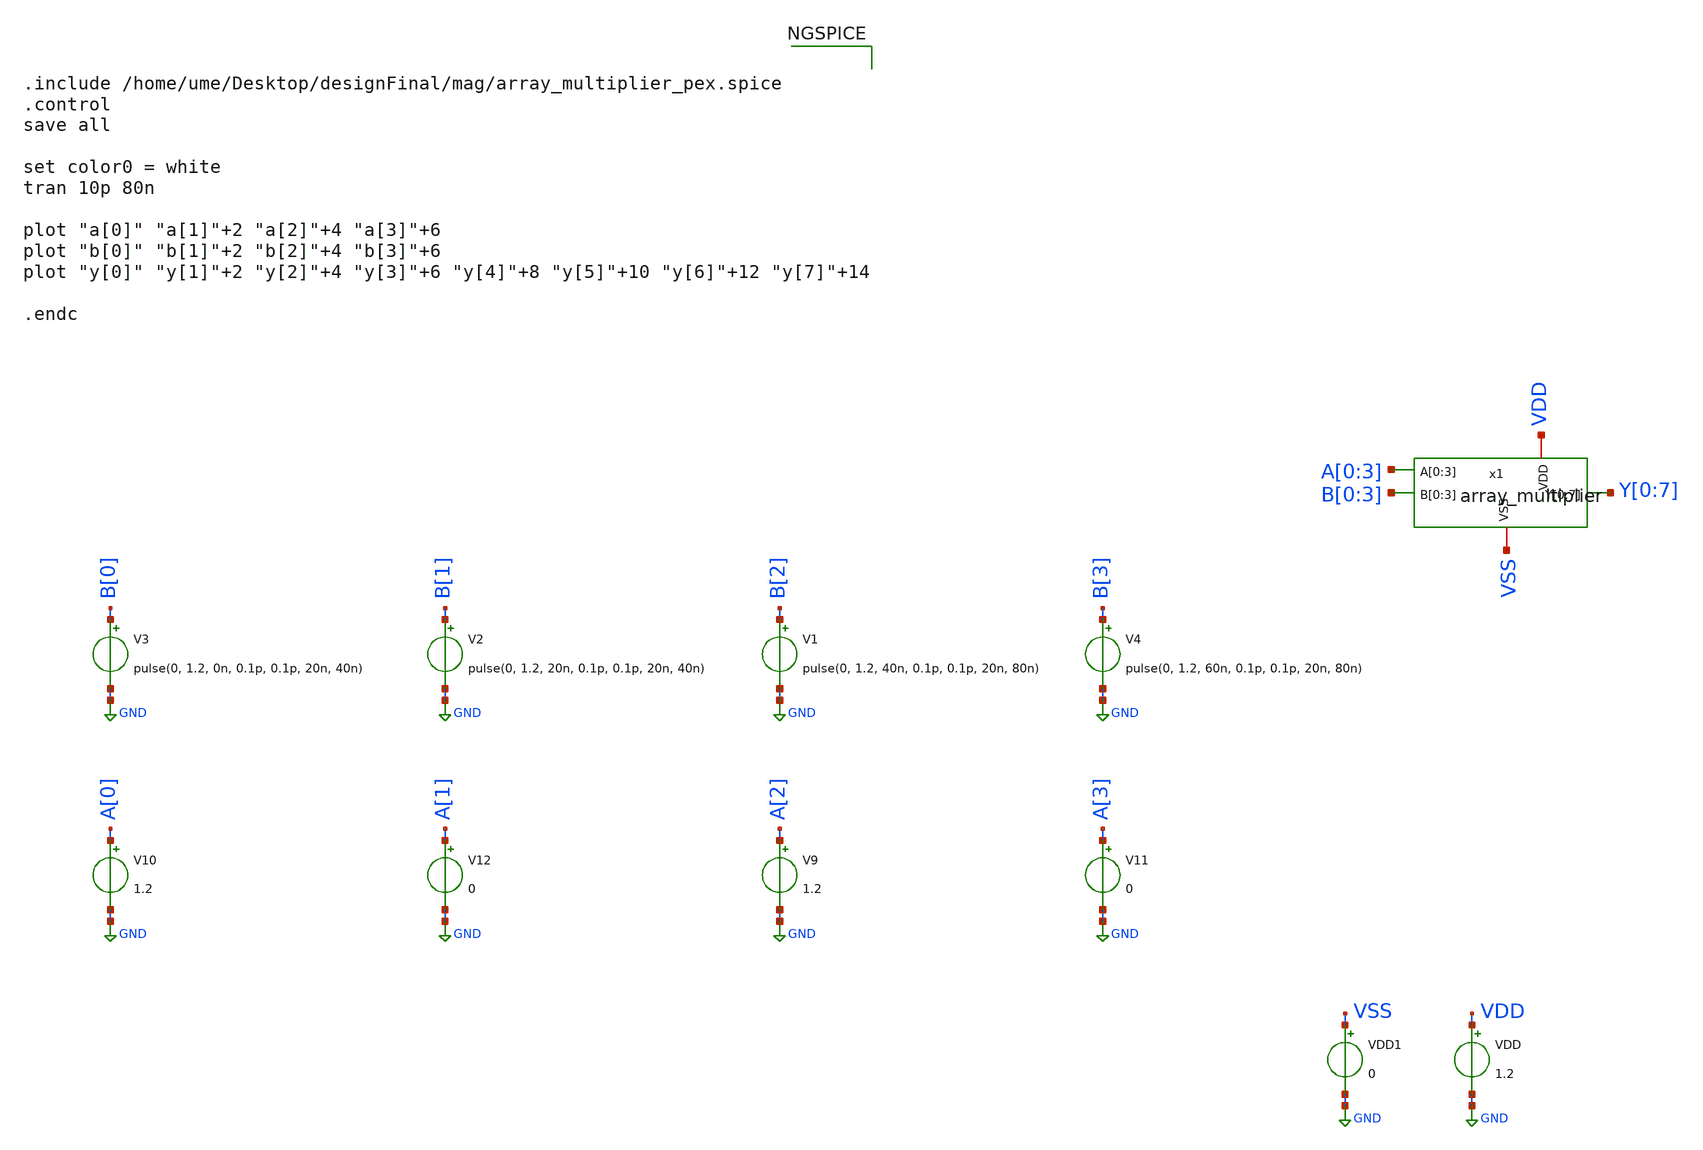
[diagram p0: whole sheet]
** sch_path: design/ALU/array_multiplayer_tb.sch
**.subckt array_multiplayer_tb
VDD VDD GND 1.2
VDD1 VSS GND 0
x1 A[0] A[1] A[2] A[3] B[0] B[1] B[2] B[3] VDD VSS Y[0] Y[1] Y[2] Y[3] Y[4] Y[5] Y[6] Y[7]
+ array_multiplier
V1 B[2] GND pulse(0, 1.2, 40n, 0.1p, 0.1p, 20n, 80n)
V4 B[3] GND pulse(0, 1.2, 60n, 0.1p, 0.1p, 20n, 80n)
V2 B[1] GND pulse(0, 1.2, 20n, 0.1p, 0.1p, 20n, 40n)
V9 A[2] GND 1.2
V11 A[3] GND 0
V12 A[1] GND 0
V10 A[0] GND 1.2
V3 B[0] GND pulse(0, 1.2, 0n, 0.1p, 0.1p, 20n, 40n)
**** begin user architecture code


.include /home/ume/Desktop/designFinal/mag/array_multiplier_pex.spice
.control
save all

set color0 = white
tran 10p 80n

plot "a[0]" "a[1]"+2 "a[2]"+4 "a[3]"+6
plot "b[0]" "b[1]"+2 "b[2]"+4 "b[3]"+6
plot "y[0]" "y[1]"+2 "y[2]"+4 "y[3]"+6 "y[4]"+8 "y[5]"+10 "y[6]"+12 "y[7]"+14

.endc


** opencircuitdesign pdks install
.lib $::SKYWATER_MODELS/sky130.lib.spice tt_mm


**** end user architecture code
**.ends
.GLOBAL GND
.end
